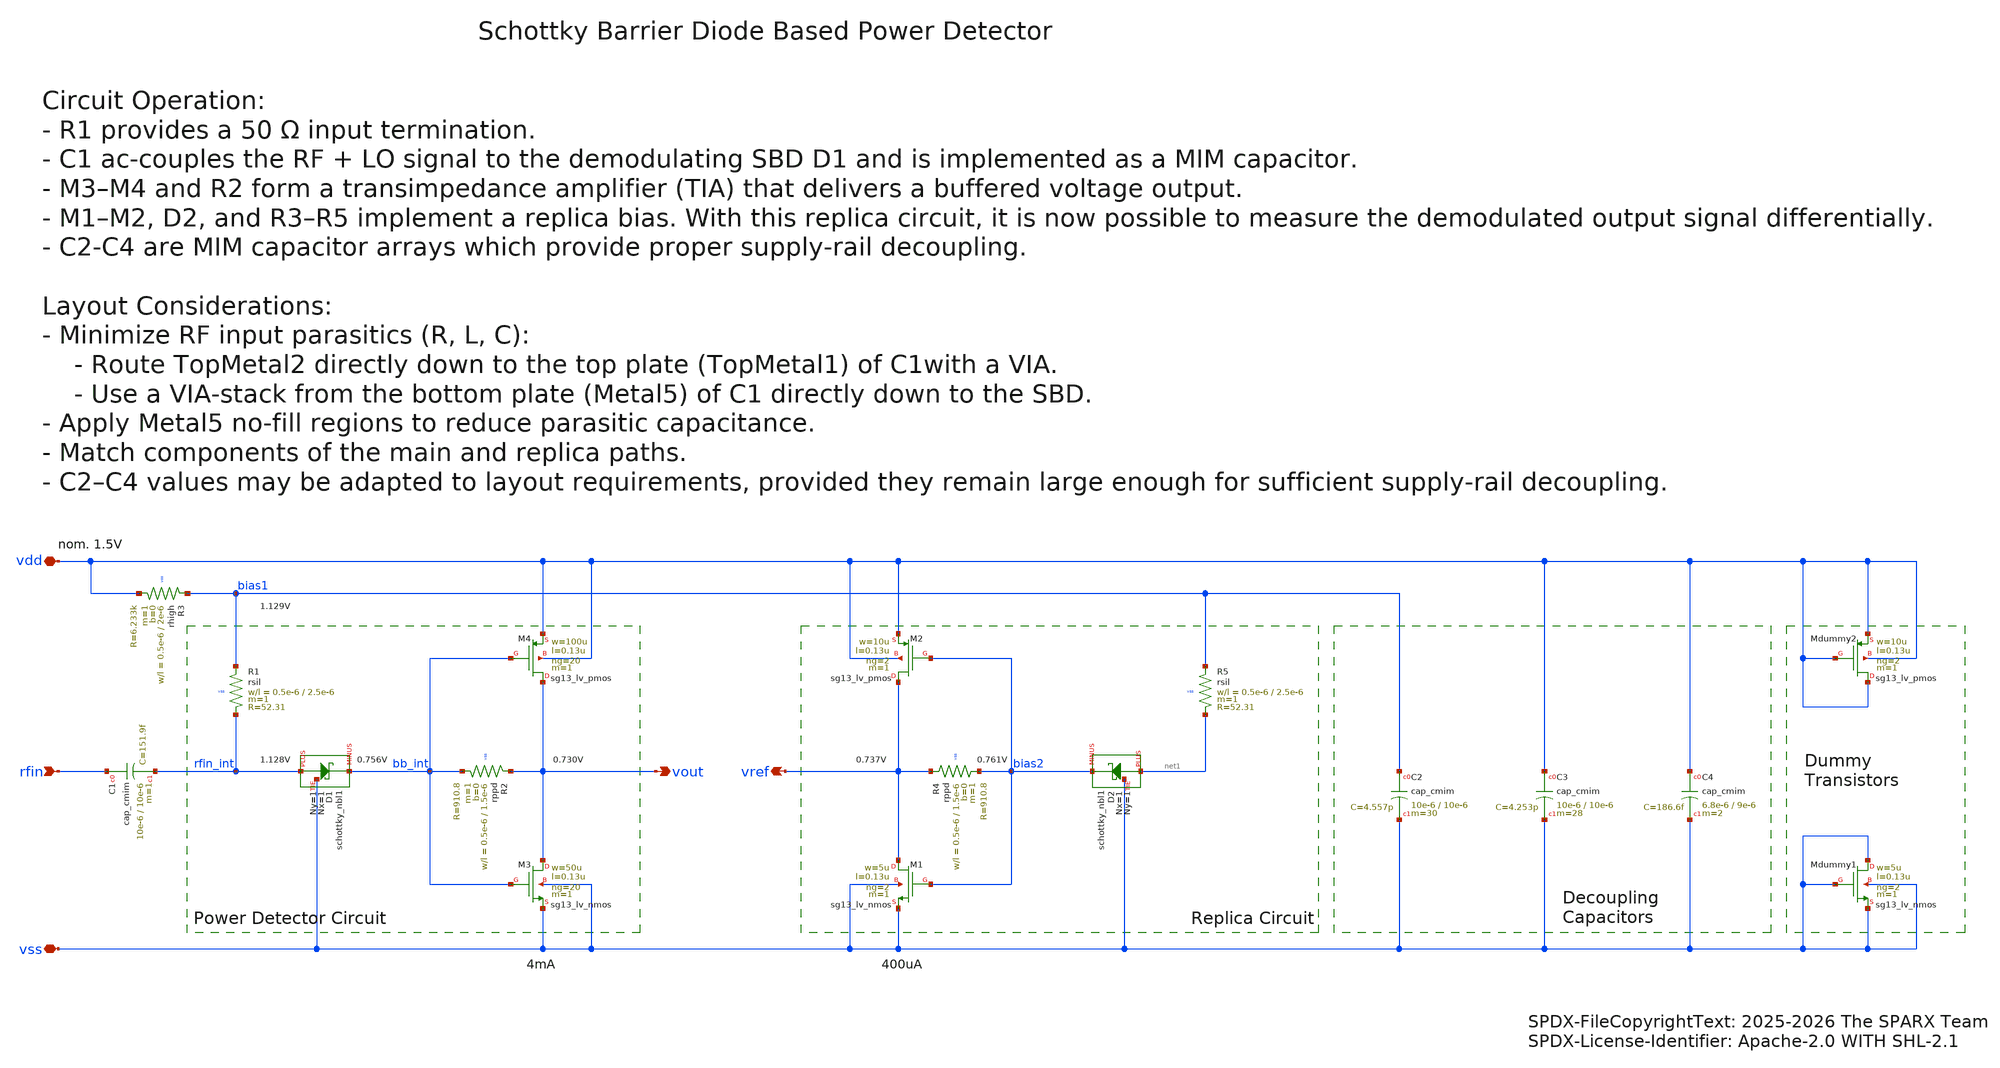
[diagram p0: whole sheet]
** sch_path: schematic/xschem/sparx_powdet_sbd.sch
* SPDX-FileCopyrightText: 2025-2026 The SPARX Team
* SPDX-License-Identifier: Apache-2.0 WITH SHL-2.1
* (c) 2026 H. Pretl, ICD@JKU
**.subckt sparx_powdet_sbd rfin vout vss vdd vref
*.ipin rfin
*.opin vout
*.iopin vss
*.iopin vdd
*.opin vref
XR1 bias1 rfin_int vss rsil w=0.5e-6 l=2.5e-6 m=1 mm_ok=1
XD1 rfin_int bb_int vss schottky_nbl1 Nx=1 Ny=1
XC2 bias1 vss cap_cmim w=10e-6 l=10e-6 m=30 mm_ok=1
XM4 vout bb_int vdd vdd sg13_lv_pmos w=100u l=0.13u ng=20 m=1 mm_ok=1
XM3 vout bb_int vss vss sg13_lv_nmos w=50u l=0.13u ng=20 m=1 mm_ok=1
XR2 vout bb_int vss rppd w=0.5e-6 l=1.5e-6 m=1 b=0 mm_ok=1
XM2 vref bias2 vdd vdd sg13_lv_pmos w=10u l=0.13u ng=2 m=1 mm_ok=1
XM1 vref bias2 vss vss sg13_lv_nmos w=5u l=0.13u ng=2 m=1 mm_ok=1
XC3 vdd vss cap_cmim w=10e-6 l=10e-6 m=28 mm_ok=1
XD2 net1 bias2 vss schottky_nbl1 Nx=1 Ny=1
XR3 bias1 vdd vss rhigh w=0.5e-6 l=2e-6 m=1 b=0 mm_ok=1
XR4 vref bias2 vss rppd w=0.5e-6 l=1.5e-6 m=1 b=0 mm_ok=1
XR5 bias1 net1 vss rsil w=0.5e-6 l=2.5e-6 m=1 mm_ok=1
XMdummy1 vss vss vss vss sg13_lv_nmos w=5u l=0.13u ng=2 m=1 mm_ok=1
XMdummy2 vdd vdd vdd vdd sg13_lv_pmos w=10u l=0.13u ng=2 m=1 mm_ok=1
XC1 rfin rfin_int cap_cmim w=10e-6 l=10e-6 m=1 mm_ok=1
XC4 vdd vss cap_cmim w=6.8e-6 l=9e-6 m=2 mm_ok=1
**.ends
.end
